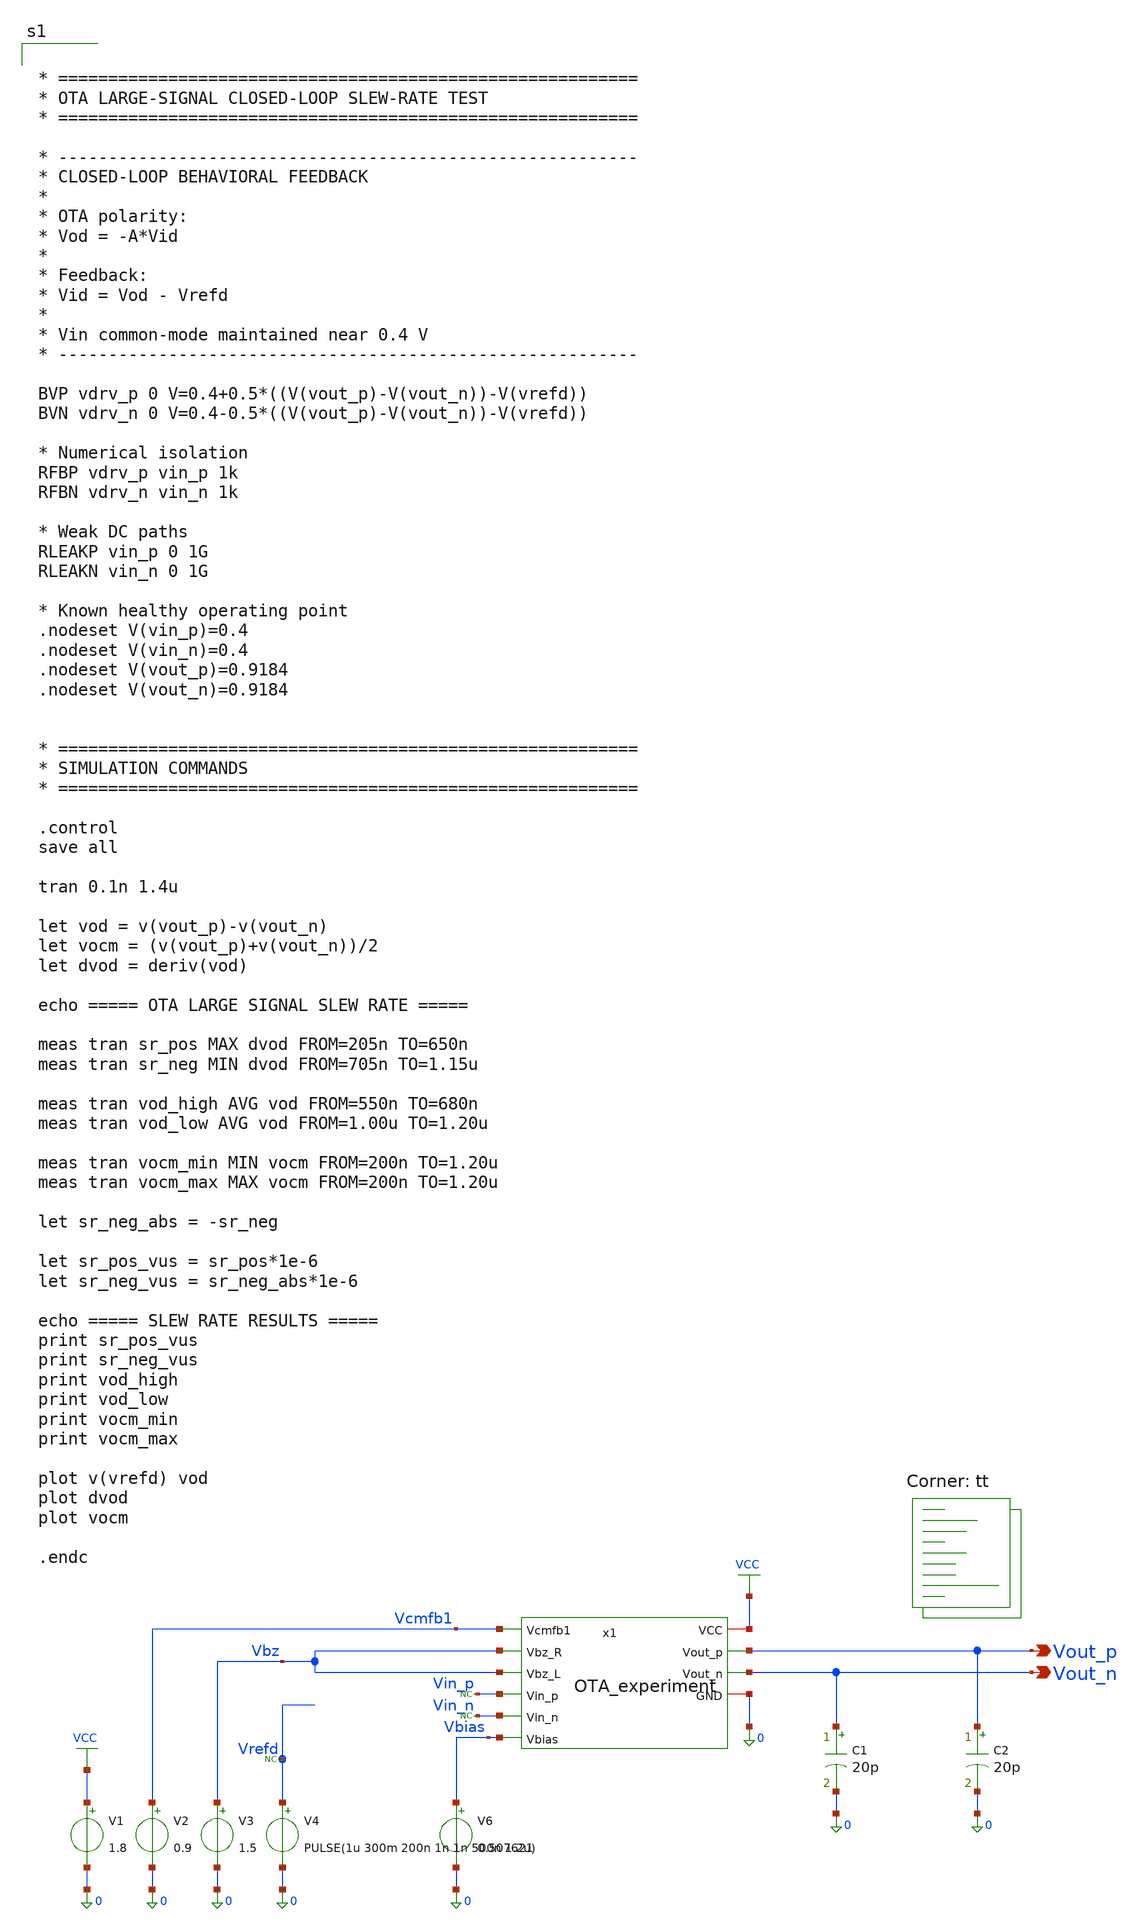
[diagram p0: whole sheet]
** sch_path: blocks/01_OTA/sim/tb_OTA_Tran_SR_experiment.sch
**.subckt tb_OTA_Tran_SR_experiment Vout_p Vout_n
*.opin Vout_p
*.opin Vout_n
V1 VCC 0 1.8
V2 Vcmfb1 0 0.9
V3 Vbz 0 1.5
V4 Vrefd 0 PULSE(1u 300m 200n 1n 1n 500n 1.2u)
V6 Vbias 0 0.507621
C1 Vout_n 0 20p m=1
C2 Vout_p 0 20p m=1
* noconn Vrefd
* noconn Vin_p
* noconn Vin_n
x1 VCC Vcmfb1 Vbz Vbz Vin_p Vin_n Vout_p Vout_n Vbias 0 OTA_experiment
**** begin user architecture code


* ==========================================================
* OTA LARGE-SIGNAL CLOSED-LOOP SLEW-RATE TEST
* ==========================================================

* ----------------------------------------------------------
* CLOSED-LOOP BEHAVIORAL FEEDBACK
*
* OTA polarity:
* Vod = -A*Vid
*
* Feedback:
* Vid = Vod - Vrefd
*
* Vin common-mode maintained near 0.4 V
* ----------------------------------------------------------

BVP vdrv_p 0 V=0.4+0.5*((V(vout_p)-V(vout_n))-V(vrefd))
BVN vdrv_n 0 V=0.4-0.5*((V(vout_p)-V(vout_n))-V(vrefd))

* Numerical isolation
RFBP vdrv_p vin_p 1k
RFBN vdrv_n vin_n 1k

* Weak DC paths
RLEAKP vin_p 0 1G
RLEAKN vin_n 0 1G

* Known healthy operating point
.nodeset V(vin_p)=0.4
.nodeset V(vin_n)=0.4
.nodeset V(vout_p)=0.9184
.nodeset V(vout_n)=0.9184


* ==========================================================
* SIMULATION COMMANDS
* ==========================================================

.control
save all

tran 0.1n 1.4u

let vod = v(vout_p)-v(vout_n)
let vocm = (v(vout_p)+v(vout_n))/2
let dvod = deriv(vod)

echo ===== OTA LARGE SIGNAL SLEW RATE =====

meas tran sr_pos MAX dvod FROM=205n TO=650n
meas tran sr_neg MIN dvod FROM=705n TO=1.15u

meas tran vod_high AVG vod FROM=550n TO=680n
meas tran vod_low AVG vod FROM=1.00u TO=1.20u

meas tran vocm_min MIN vocm FROM=200n TO=1.20u
meas tran vocm_max MAX vocm FROM=200n TO=1.20u

let sr_neg_abs = -sr_neg

let sr_pos_vus = sr_pos*1e-6
let sr_neg_vus = sr_neg_abs*1e-6

echo ===== SLEW RATE RESULTS =====
print sr_pos_vus
print sr_neg_vus
print vod_high
print vod_low
print vocm_min
print vocm_max

plot v(vrefd) vod
plot dvod
plot vocm

.endc


.lib $::SKYWATER_MODELS/sky130.lib.spice tt
**** end user architecture code
**.ends

* expanding   symbol:  blocks/01_OTA/xschem/OTA_experiment.sym # of pins=10
** sym_path: blocks/01_OTA/xschem/OTA_experiment.sym
** sch_path: blocks/01_OTA/xschem/OTA_experiment.sch
.subckt OTA_experiment VCC Vcmfb1 Vbz_R Vbz_L Vin_p Vin_n Vout_p Vout_n Vbias GND
*.ipin Vin_p
*.ipin Vin_n
*.ipin Vbias
*.ipin Vbz_R
*.ipin Vbz_L
*.ipin Vcmfb1
*.opin Vout_p
*.opin Vout_n
*.iopin VCC
*.iopin GND
XM1 net5 Vin_p net3 net5 sky130_fd_pr__pfet_01v8 L=1.2 W=120 nf=1 ad='int((1 + 1)/2) * 120 / 1 * 0.29'
+ as='int((1 + 2)/2) * 120 / 1 * 0.29' pd='2*int((1 + 1)/2) * (120 / 1 + 0.29)' ps='2*int((1 + 2)/2) * (120 / 1 + 0.29)'
+ nrd='0.29 / 120 ' nrs='0.29 / 120 ' sa=0 sb=0 sd=0 mult=1 m=1
XM2 net5 Vin_n net4 net5 sky130_fd_pr__pfet_01v8 L=1.2 W=120 nf=1 ad='int((1 + 1)/2) * 120 / 1 * 0.29'
+ as='int((1 + 2)/2) * 120 / 1 * 0.29' pd='2*int((1 + 1)/2) * (120 / 1 + 0.29)' ps='2*int((1 + 2)/2) * (120 / 1 + 0.29)'
+ nrd='0.29 / 120 ' nrs='0.29 / 120 ' sa=0 sb=0 sd=0 mult=1 m=1
XM3 net3 Vbias GND GND sky130_fd_pr__nfet_01v8 L=2 W=8 nf=1 ad='int((1 + 1)/2) * 8 / 1 * 0.29' as='int((1 + 2)/2) * 8 / 1 * 0.29'
+ pd='2*int((1 + 1)/2) * (8 / 1 + 0.29)' ps='2*int((1 + 2)/2) * (8 / 1 + 0.29)' nrd='0.29 / 8 ' nrs='0.29 / 8 '
+ sa=0 sb=0 sd=0 mult=1 m=1
XM4 net4 Vbias GND GND sky130_fd_pr__nfet_01v8 L=2 W=8 nf=1 ad='int((1 + 1)/2) * 8 / 1 * 0.29' as='int((1 + 2)/2) * 8 / 1 * 0.29'
+ pd='2*int((1 + 1)/2) * (8 / 1 + 0.29)' ps='2*int((1 + 2)/2) * (8 / 1 + 0.29)' nrd='0.29 / 8 ' nrs='0.29 / 8 '
+ sa=0 sb=0 sd=0 mult=1 m=1
XM5 net1 net4 GND GND sky130_fd_pr__nfet_01v8 L=2 W=20 nf=1 ad='int((1 + 1)/2) * 20 / 1 * 0.29' as='int((1 + 2)/2) * 20 / 1 * 0.29'
+ pd='2*int((1 + 1)/2) * (20 / 1 + 0.29)' ps='2*int((1 + 2)/2) * (20 / 1 + 0.29)' nrd='0.29 / 20 ' nrs='0.29 / 20 '
+ sa=0 sb=0 sd=0 mult=1 m=1
XM6 net2 net3 GND GND sky130_fd_pr__nfet_01v8 L=2 W=20 nf=1 ad='int((1 + 1)/2) * 20 / 1 * 0.29' as='int((1 + 2)/2) * 20 / 1 * 0.29'
+ pd='2*int((1 + 1)/2) * (20 / 1 + 0.29)' ps='2*int((1 + 2)/2) * (20 / 1 + 0.29)' nrd='0.29 / 20 ' nrs='0.29 / 20 '
+ sa=0 sb=0 sd=0 mult=1 m=1
XM7 VCC net1 net1 VCC sky130_fd_pr__pfet_01v8 L=2 W=30 nf=1 ad='int((1 + 1)/2) * 30 / 1 * 0.29' as='int((1 + 2)/2) * 30 / 1 * 0.29'
+ pd='2*int((1 + 1)/2) * (30 / 1 + 0.29)' ps='2*int((1 + 2)/2) * (30 / 1 + 0.29)' nrd='0.29 / 30 ' nrs='0.29 / 30 '
+ sa=0 sb=0 sd=0 mult=1 m=1
XM8 VCC net2 net2 VCC sky130_fd_pr__pfet_01v8 L=2 W=30 nf=1 ad='int((1 + 1)/2) * 30 / 1 * 0.29' as='int((1 + 2)/2) * 30 / 1 * 0.29'
+ pd='2*int((1 + 1)/2) * (30 / 1 + 0.29)' ps='2*int((1 + 2)/2) * (30 / 1 + 0.29)' nrd='0.29 / 30 ' nrs='0.29 / 30 '
+ sa=0 sb=0 sd=0 mult=1 m=1
XM9 VCC net1 Vout_p VCC sky130_fd_pr__pfet_01v8 L=1 W=300 nf=1 ad='int((1 + 1)/2) * 300 / 1 * 0.29' as='int((1 + 2)/2) * 300 / 1 * 0.29'
+ pd='2*int((1 + 1)/2) * (300 / 1 + 0.29)' ps='2*int((1 + 2)/2) * (300 / 1 + 0.29)' nrd='0.29 / 300 ' nrs='0.29 / 300 '
+ sa=0 sb=0 sd=0 mult=1 m=1
XM10 VCC net2 Vout_n VCC sky130_fd_pr__pfet_01v8 L=1 W=300 nf=1 ad='int((1 + 1)/2) * 300 / 1 * 0.29'
+ as='int((1 + 2)/2) * 300 / 1 * 0.29' pd='2*int((1 + 1)/2) * (300 / 1 + 0.29)' ps='2*int((1 + 2)/2) * (300 / 1 + 0.29)'
+ nrd='0.29 / 300 ' nrs='0.29 / 300 ' sa=0 sb=0 sd=0 mult=1 m=1
XM11 Vout_p net4 GND GND sky130_fd_pr__nfet_01v8 L=1 W=200 nf=1 ad='int((1 + 1)/2) * 200 / 1 * 0.29'
+ as='int((1 + 2)/2) * 200 / 1 * 0.29' pd='2*int((1 + 1)/2) * (200 / 1 + 0.29)' ps='2*int((1 + 2)/2) * (200 / 1 + 0.29)'
+ nrd='0.29 / 200 ' nrs='0.29 / 200 ' sa=0 sb=0 sd=0 mult=1 m=1
XM12 Vout_n net3 GND GND sky130_fd_pr__nfet_01v8 L=1 W=200 nf=1 ad='int((1 + 1)/2) * 200 / 1 * 0.29'
+ as='int((1 + 2)/2) * 200 / 1 * 0.29' pd='2*int((1 + 1)/2) * (200 / 1 + 0.29)' ps='2*int((1 + 2)/2) * (200 / 1 + 0.29)'
+ nrd='0.29 / 200 ' nrs='0.29 / 200 ' sa=0 sb=0 sd=0 mult=1 m=1
XM13 VCC Vcmfb1 net5 VCC sky130_fd_pr__pfet_01v8 L=1.2 W=60 nf=1 ad='int((1 + 1)/2) * 60 / 1 * 0.29'
+ as='int((1 + 2)/2) * 60 / 1 * 0.29' pd='2*int((1 + 1)/2) * (60 / 1 + 0.29)' ps='2*int((1 + 2)/2) * (60 / 1 + 0.29)'
+ nrd='0.29 / 60 ' nrs='0.29 / 60 ' sa=0 sb=0 sd=0 mult=1 m=1
XC1 Vout_p net4 sky130_fd_pr__cap_mim_m3_1 W=1 L=1 MF=80 m=80
XC2 net3 Vout_n sky130_fd_pr__cap_mim_m3_1 W=1 L=1 MF=80 m=80
.ends

.GLOBAL VCC
.end
